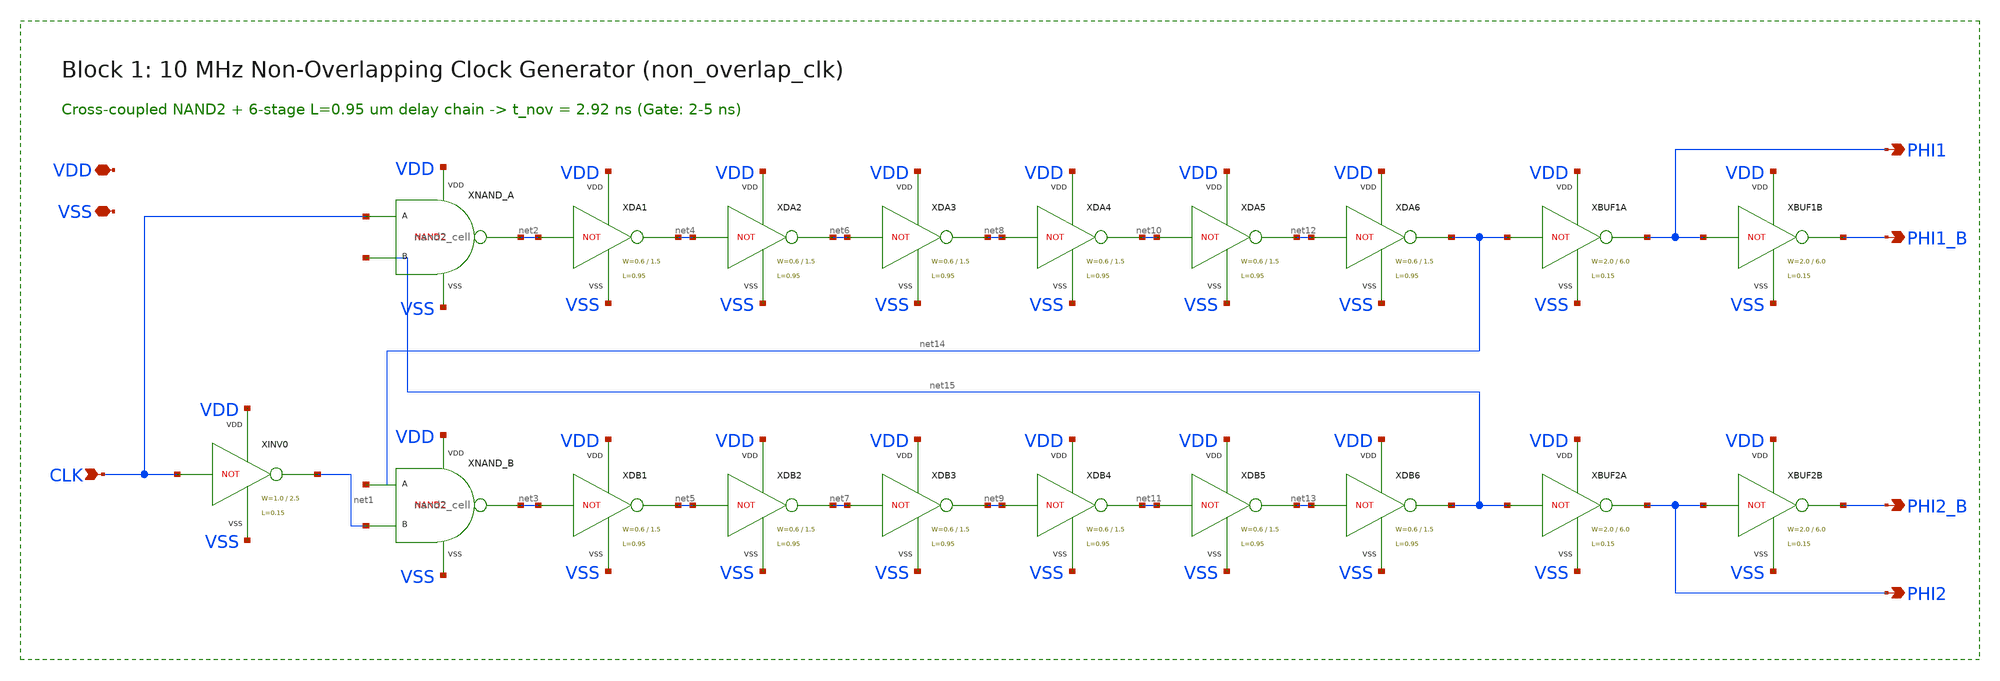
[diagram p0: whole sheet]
** sch_path: sky130-sc-lpf/xschem/non_overlap_clk.sch
**.subckt non_overlap_clk VDD VSS CLK PHI1 PHI1_B PHI2 PHI2_B
*.iopin VDD
*.iopin VSS
*.ipin CLK
*.opin PHI1
*.opin PHI1_B
*.opin PHI2
*.opin PHI2_B
XINV0 CLK net1 VDD VSS inv_cell WN=1.0 WP=2.5 LCH=0.15
XNAND_A CLK net15 net2 VDD VSS nand2_cell
XNAND_B net14 net1 net3 VDD VSS nand2_cell
XDA1 net2 net4 VDD VSS inv_cell WN=0.6 WP=1.5 LCH=0.95
XDB1 net3 net5 VDD VSS inv_cell WN=0.6 WP=1.5 LCH=0.95
XDA2 net4 net6 VDD VSS inv_cell WN=0.6 WP=1.5 LCH=0.95
XDB2 net5 net7 VDD VSS inv_cell WN=0.6 WP=1.5 LCH=0.95
XDA3 net6 net8 VDD VSS inv_cell WN=0.6 WP=1.5 LCH=0.95
XDB3 net7 net9 VDD VSS inv_cell WN=0.6 WP=1.5 LCH=0.95
XDA4 net8 net10 VDD VSS inv_cell WN=0.6 WP=1.5 LCH=0.95
XDB4 net9 net11 VDD VSS inv_cell WN=0.6 WP=1.5 LCH=0.95
XDA5 net10 net12 VDD VSS inv_cell WN=0.6 WP=1.5 LCH=0.95
XDB5 net11 net13 VDD VSS inv_cell WN=0.6 WP=1.5 LCH=0.95
XDA6 net12 net14 VDD VSS inv_cell WN=0.6 WP=1.5 LCH=0.95
XDB6 net13 net15 VDD VSS inv_cell WN=0.6 WP=1.5 LCH=0.95
XBUF1A net14 PHI1 VDD VSS inv_cell WN=2.0 WP=6.0 LCH=0.15
XBUF1B PHI1 PHI1_B VDD VSS inv_cell WN=2.0 WP=6.0 LCH=0.15
XBUF2A net15 PHI2 VDD VSS inv_cell WN=2.0 WP=6.0 LCH=0.15
XBUF2B PHI2 PHI2_B VDD VSS inv_cell WN=2.0 WP=6.0 LCH=0.15
**.ends

* expanding   symbol:  inv_cell.sym # of pins=4
** sym_path: sky130-sc-lpf/xschem/inv_cell.sym
** sch_path: sky130-sc-lpf/xschem/inv_cell.sch
.subckt inv_cell A Y VDD VSS  WN=1.0 WP=2.5 LCH=0.15
*.ipin A
*.opin Y
*.iopin VDD
*.iopin VSS
XMP Y A VDD VDD sky130_fd_pr__pfet_01v8 L='LCH' W='WP' nf=1 ad='WP*0.29' as='WP*0.29' pd='2*(WP+0.29)'
+ ps='2*(WP+0.29)' nrd='0.29/WP' nrs='0.29/WP' sa=0 sb=0 sd=0 mult=1 m=1
XMN Y A VSS VSS sky130_fd_pr__nfet_01v8 L='LCH' W='WN' nf=1 ad='WN*0.29' as='WN*0.29' pd='2*(WN+0.29)'
+ ps='2*(WN+0.29)' nrd='0.29/WN' nrs='0.29/WN' sa=0 sb=0 sd=0 mult=1 m=1
.ends


* expanding   symbol:  nand2_cell.sym # of pins=5
** sym_path: sky130-sc-lpf/xschem/nand2_cell.sym
** sch_path: sky130-sc-lpf/xschem/nand2_cell.sch
.subckt nand2_cell A B Y VDD VSS
*.iopin VDD
*.opin Y
*.iopin VSS
*.ipin A
*.ipin B
XMPA Y A VDD VDD sky130_fd_pr__pfet_01v8 L=0.15 W=2.0 nf=1 ad='int((nf+1)/2) * W/nf * 0.29' as='int((nf+2)/2) * W/nf * 0.29'
+ pd='2*int((nf+1)/2) * (W/nf + 0.29)' ps='2*int((nf+2)/2) * (W/nf + 0.29)' nrd='0.29 / W' nrs='0.29 / W'
+ sa=0 sb=0 sd=0 mult=1 m=1
XMPB Y B VDD VDD sky130_fd_pr__pfet_01v8 L=0.15 W=2.0 nf=1 ad='int((nf+1)/2) * W/nf * 0.29' as='int((nf+2)/2) * W/nf * 0.29'
+ pd='2*int((nf+1)/2) * (W/nf + 0.29)' ps='2*int((nf+2)/2) * (W/nf + 0.29)' nrd='0.29 / W' nrs='0.29 / W'
+ sa=0 sb=0 sd=0 mult=1 m=1
XMNA Y A net1 VSS sky130_fd_pr__nfet_01v8 L=0.15 W=1.6 nf=1 ad='int((1 + 1)/2) * 1.6 / 1 * 0.29' as='int((1 + 2)/2) * 1.6 / 1 * 0.29'
+ pd='2*int((1 + 1)/2) * (1.6 / 1 + 0.29)' ps='2*int((1 + 2)/2) * (1.6 / 1 + 0.29)' nrd='0.29 / 1.6 ' nrs='0.29 / 1.6 '
+ sa=0 sb=0 sd=0 mult=1 m=1
XMNB net1 B VSS VSS sky130_fd_pr__nfet_01v8 L=0.15 W=1.6 nf=1 ad='int((1 + 1)/2) * 1.6 / 1 * 0.29' as='int((1 + 2)/2) * 1.6 / 1 * 0.29'
+ pd='2*int((1 + 1)/2) * (1.6 / 1 + 0.29)' ps='2*int((1 + 2)/2) * (1.6 / 1 + 0.29)' nrd='0.29 / 1.6 ' nrs='0.29 / 1.6 '
+ sa=0 sb=0 sd=0 mult=1 m=1
.ends

.end
